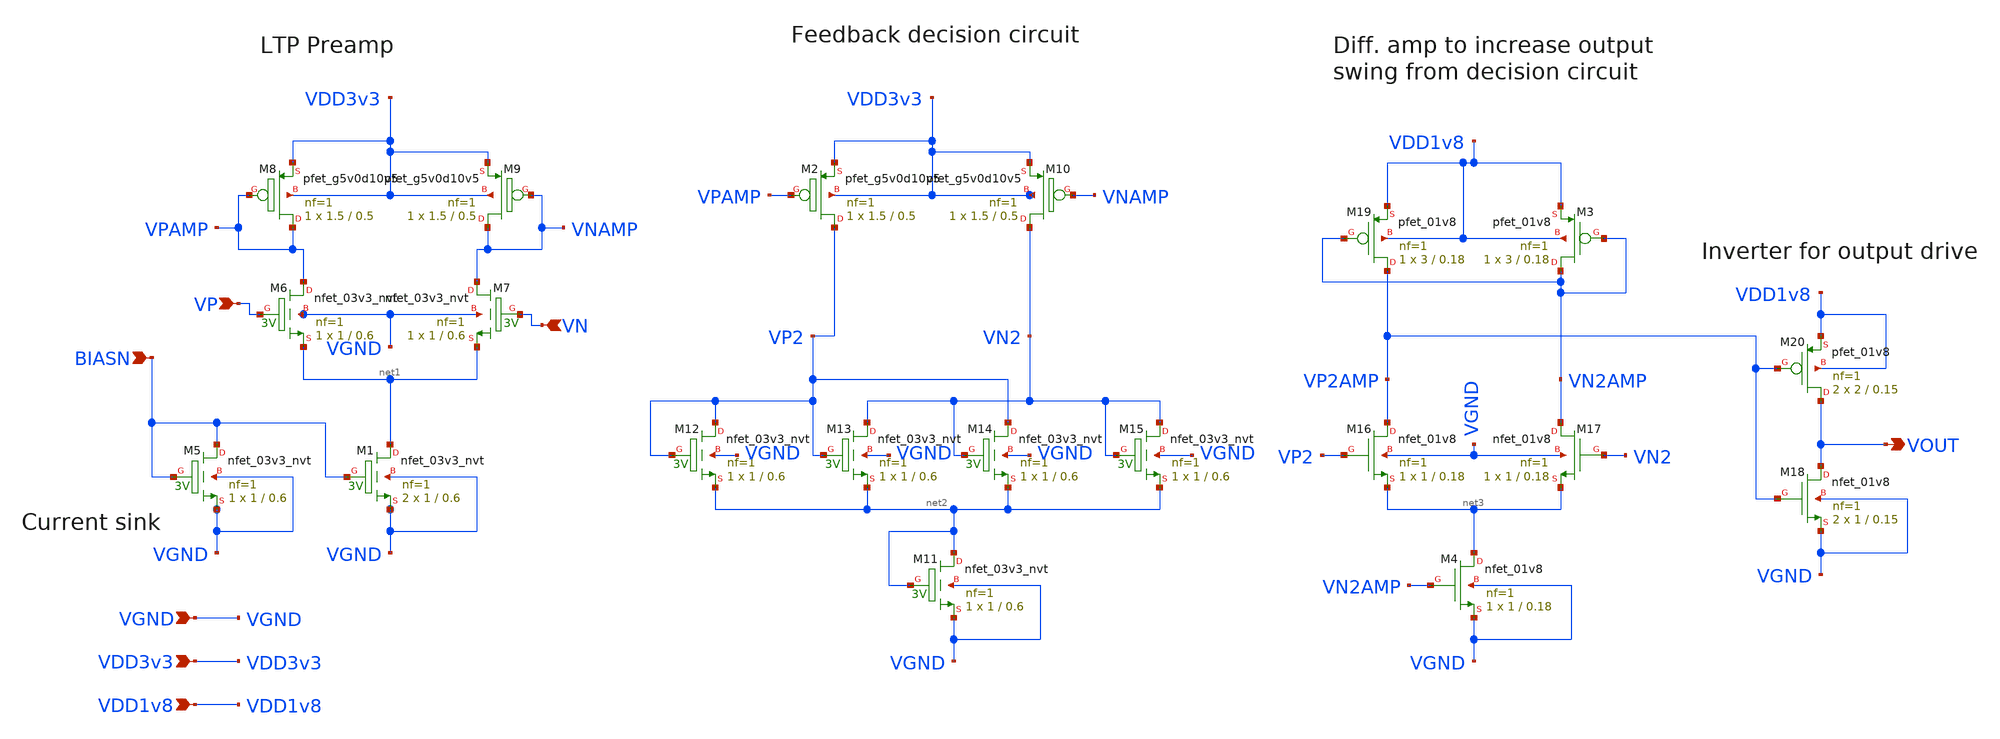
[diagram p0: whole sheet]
** sch_path: xschem/sar_adc/comparator.sch
**.subckt comparator BIASN VP VN VOUT VGND VDD3v3 VDD1v8
*.ipin BIASN
*.ipin VP
*.ipin VN
*.opin VOUT
*.ipin VGND
*.ipin VDD3v3
*.ipin VDD1v8
XM2 VP2 VPAMP VDD3v3 VDD3v3 sky130_fd_pr__pfet_g5v0d10v5 L=0.5 W=1.5 nf=1 ad='int((nf+1)/2) * W/nf * 0.29'
+ as='int((nf+2)/2) * W/nf * 0.29' pd='2*int((nf+1)/2) * (W/nf + 0.29)' ps='2*int((nf+2)/2) * (W/nf + 0.29)'
+ nrd='0.29 / W' nrs='0.29 / W' sa=0 sb=0 sd=0 mult=1 m=1
XM3 VN2AMP VN2AMP VDD1v8 VDD1v8 sky130_fd_pr__pfet_01v8 L=0.18 W=3 nf=1 ad='int((nf+1)/2) * W/nf * 0.29'
+ as='int((nf+2)/2) * W/nf * 0.29' pd='2*int((nf+1)/2) * (W/nf + 0.29)' ps='2*int((nf+2)/2) * (W/nf + 0.29)'
+ nrd='0.29 / W' nrs='0.29 / W' sa=0 sb=0 sd=0 mult=1 m=1
XM4 net3 VN2AMP VGND VGND sky130_fd_pr__nfet_01v8 L=0.18 W=1 nf=1 ad='int((nf+1)/2) * W/nf * 0.29' as='int((nf+2)/2) * W/nf * 0.29'
+ pd='2*int((nf+1)/2) * (W/nf + 0.29)' ps='2*int((nf+2)/2) * (W/nf + 0.29)' nrd='0.29 / W' nrs='0.29 / W'
+ sa=0 sb=0 sd=0 mult=1 m=1
XM5 BIASN BIASN VGND VGND sky130_fd_pr__nfet_03v3_nvt L=0.6 W=1 nf=1 ad='int((nf+1)/2) * W/nf * 0.29'
+ as='int((nf+2)/2) * W/nf * 0.29' pd='2*int((nf+1)/2) * (W/nf + 0.29)' ps='2*int((nf+2)/2) * (W/nf + 0.29)'
+ nrd='0.29 / W' nrs='0.29 / W' sa=0 sb=0 sd=0 mult=1 m=1
XM1 net1 BIASN VGND VGND sky130_fd_pr__nfet_03v3_nvt L=0.6 W=1 nf=1 ad='int((nf+1)/2) * W/nf * 0.29'
+ as='int((nf+2)/2) * W/nf * 0.29' pd='2*int((nf+1)/2) * (W/nf + 0.29)' ps='2*int((nf+2)/2) * (W/nf + 0.29)'
+ nrd='0.29 / W' nrs='0.29 / W' sa=0 sb=0 sd=0 mult=2 m=2
XM6 VPAMP VP net1 VGND sky130_fd_pr__nfet_03v3_nvt L=0.6 W=1 nf=1 ad='int((nf+1)/2) * W/nf * 0.29' as='int((nf+2)/2) * W/nf * 0.29'
+ pd='2*int((nf+1)/2) * (W/nf + 0.29)' ps='2*int((nf+2)/2) * (W/nf + 0.29)' nrd='0.29 / W' nrs='0.29 / W'
+ sa=0 sb=0 sd=0 mult=1 m=1
XM7 VNAMP VN net1 VGND sky130_fd_pr__nfet_03v3_nvt L=0.6 W=1 nf=1 ad='int((nf+1)/2) * W/nf * 0.29' as='int((nf+2)/2) * W/nf * 0.29'
+ pd='2*int((nf+1)/2) * (W/nf + 0.29)' ps='2*int((nf+2)/2) * (W/nf + 0.29)' nrd='0.29 / W' nrs='0.29 / W'
+ sa=0 sb=0 sd=0 mult=1 m=1
XM8 VPAMP VPAMP VDD3v3 VDD3v3 sky130_fd_pr__pfet_g5v0d10v5 L=0.5 W=1.5 nf=1 ad='int((nf+1)/2) * W/nf * 0.29'
+ as='int((nf+2)/2) * W/nf * 0.29' pd='2*int((nf+1)/2) * (W/nf + 0.29)' ps='2*int((nf+2)/2) * (W/nf + 0.29)'
+ nrd='0.29 / W' nrs='0.29 / W' sa=0 sb=0 sd=0 mult=1 m=1
XM9 VNAMP VNAMP VDD3v3 VDD3v3 sky130_fd_pr__pfet_g5v0d10v5 L=0.5 W=1.5 nf=1 ad='int((nf+1)/2) * W/nf * 0.29'
+ as='int((nf+2)/2) * W/nf * 0.29' pd='2*int((nf+1)/2) * (W/nf + 0.29)' ps='2*int((nf+2)/2) * (W/nf + 0.29)'
+ nrd='0.29 / W' nrs='0.29 / W' sa=0 sb=0 sd=0 mult=1 m=1
XM10 VN2 VNAMP VDD3v3 VDD3v3 sky130_fd_pr__pfet_g5v0d10v5 L=0.5 W=1.5 nf=1 ad='int((nf+1)/2) * W/nf * 0.29'
+ as='int((nf+2)/2) * W/nf * 0.29' pd='2*int((nf+1)/2) * (W/nf + 0.29)' ps='2*int((nf+2)/2) * (W/nf + 0.29)'
+ nrd='0.29 / W' nrs='0.29 / W' sa=0 sb=0 sd=0 mult=1 m=1
XM12 VP2 VP2 net2 VGND sky130_fd_pr__nfet_03v3_nvt L=0.6 W=1 nf=1 ad='int((nf+1)/2) * W/nf * 0.29' as='int((nf+2)/2) * W/nf * 0.29'
+ pd='2*int((nf+1)/2) * (W/nf + 0.29)' ps='2*int((nf+2)/2) * (W/nf + 0.29)' nrd='0.29 / W' nrs='0.29 / W'
+ sa=0 sb=0 sd=0 mult=1 m=1
XM11 net2 net2 VGND VGND sky130_fd_pr__nfet_03v3_nvt L=0.6 W=1 nf=1 ad='int((nf+1)/2) * W/nf * 0.29'
+ as='int((nf+2)/2) * W/nf * 0.29' pd='2*int((nf+1)/2) * (W/nf + 0.29)' ps='2*int((nf+2)/2) * (W/nf + 0.29)'
+ nrd='0.29 / W' nrs='0.29 / W' sa=0 sb=0 sd=0 mult=1 m=1
XM13 VN2 VP2 net2 VGND sky130_fd_pr__nfet_03v3_nvt L=0.6 W=1 nf=1 ad='int((nf+1)/2) * W/nf * 0.29' as='int((nf+2)/2) * W/nf * 0.29'
+ pd='2*int((nf+1)/2) * (W/nf + 0.29)' ps='2*int((nf+2)/2) * (W/nf + 0.29)' nrd='0.29 / W' nrs='0.29 / W'
+ sa=0 sb=0 sd=0 mult=1 m=1
XM14 VP2 VN2 net2 VGND sky130_fd_pr__nfet_03v3_nvt L=0.6 W=1 nf=1 ad='int((nf+1)/2) * W/nf * 0.29' as='int((nf+2)/2) * W/nf * 0.29'
+ pd='2*int((nf+1)/2) * (W/nf + 0.29)' ps='2*int((nf+2)/2) * (W/nf + 0.29)' nrd='0.29 / W' nrs='0.29 / W'
+ sa=0 sb=0 sd=0 mult=1 m=1
XM15 VN2 VN2 net2 VGND sky130_fd_pr__nfet_03v3_nvt L=0.6 W=1 nf=1 ad='int((nf+1)/2) * W/nf * 0.29' as='int((nf+2)/2) * W/nf * 0.29'
+ pd='2*int((nf+1)/2) * (W/nf + 0.29)' ps='2*int((nf+2)/2) * (W/nf + 0.29)' nrd='0.29 / W' nrs='0.29 / W'
+ sa=0 sb=0 sd=0 mult=1 m=1
XM16 VP2AMP VP2 net3 VGND sky130_fd_pr__nfet_01v8 L=0.18 W=1 nf=1 ad='int((nf+1)/2) * W/nf * 0.29' as='int((nf+2)/2) * W/nf * 0.29'
+ pd='2*int((nf+1)/2) * (W/nf + 0.29)' ps='2*int((nf+2)/2) * (W/nf + 0.29)' nrd='0.29 / W' nrs='0.29 / W'
+ sa=0 sb=0 sd=0 mult=1 m=1
XM17 VN2AMP VN2 net3 VGND sky130_fd_pr__nfet_01v8 L=0.18 W=1 nf=1 ad='int((nf+1)/2) * W/nf * 0.29' as='int((nf+2)/2) * W/nf * 0.29'
+ pd='2*int((nf+1)/2) * (W/nf + 0.29)' ps='2*int((nf+2)/2) * (W/nf + 0.29)' nrd='0.29 / W' nrs='0.29 / W'
+ sa=0 sb=0 sd=0 mult=1 m=1
XM18 VOUT VP2AMP VGND VGND sky130_fd_pr__nfet_01v8 L=0.15 W=1 nf=1 ad='int((nf+1)/2) * W/nf * 0.29' as='int((nf+2)/2) * W/nf * 0.29'
+ pd='2*int((nf+1)/2) * (W/nf + 0.29)' ps='2*int((nf+2)/2) * (W/nf + 0.29)' nrd='0.29 / W' nrs='0.29 / W'
+ sa=0 sb=0 sd=0 mult=2 m=2
XM19 VP2AMP VN2AMP VDD1v8 VDD1v8 sky130_fd_pr__pfet_01v8 L=0.18 W=3 nf=1 ad='int((nf+1)/2) * W/nf * 0.29'
+ as='int((nf+2)/2) * W/nf * 0.29' pd='2*int((nf+1)/2) * (W/nf + 0.29)' ps='2*int((nf+2)/2) * (W/nf + 0.29)'
+ nrd='0.29 / W' nrs='0.29 / W' sa=0 sb=0 sd=0 mult=1 m=1
XM20 VOUT VP2AMP VDD1v8 VDD1v8 sky130_fd_pr__pfet_01v8 L=0.15 W=2 nf=1 ad='int((nf+1)/2) * W/nf * 0.29'
+ as='int((nf+2)/2) * W/nf * 0.29' pd='2*int((nf+1)/2) * (W/nf + 0.29)' ps='2*int((nf+2)/2) * (W/nf + 0.29)'
+ nrd='0.29 / W' nrs='0.29 / W' sa=0 sb=0 sd=0 mult=2 m=2
**.ends
.end
